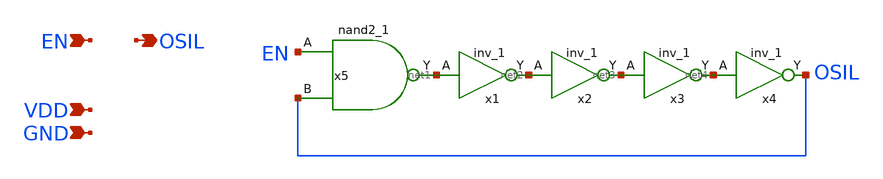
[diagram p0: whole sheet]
** sch_path: hgu/tutorial_jh/ring.sch
**.subckt ring EN OSIL GND VDD
*.ipin EN
*.opin OSIL
*.ipin GND
*.ipin VDD
x1 net1 GND GND VDD VDD net2 sky130_fd_sc_hd__inv_1
x5 EN OSIL GND GND VDD VDD net1 sky130_fd_sc_hd__nand2_1
x2 net2 GND GND VDD VDD net3 sky130_fd_sc_hd__inv_1
x3 net3 GND GND VDD VDD net4 sky130_fd_sc_hd__inv_1
x4 net4 GND GND VDD VDD OSIL sky130_fd_sc_hd__inv_1
**.ends
.end
